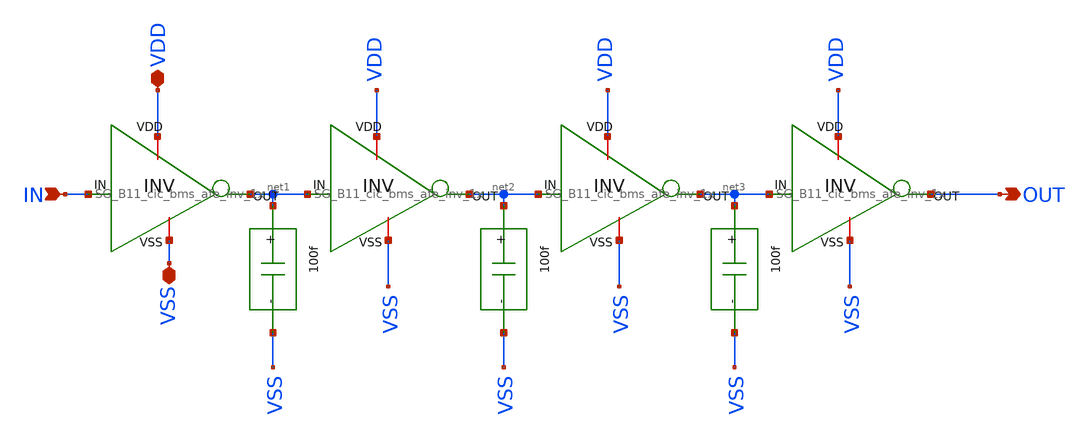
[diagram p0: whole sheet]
** sch_path: design/schematics/CCIA/Non_Overlapping_clk_gen/SG_B11_cic_bms_afe_delay_block_3n.sch
**.subckt SG_B11_cic_bms_afe_delay_block_3n IN OUT VDD VSS
*.ipin IN
*.opin OUT
*.iopin VDD
*.iopin VSS
x1 VDD net1 IN VSS SG_B11_cic_bms_afe_inv_1x
x2 VDD net2 net1 VSS SG_B11_cic_bms_afe_inv_1x
x3 VDD net3 net2 VSS SG_B11_cic_bms_afe_inv_1x
x4 VDD OUT net3 VSS SG_B11_cic_bms_afe_inv_1x
x5 net1 VSS SG_B11_cic_bms_afe_delay_3n_cap
x6 net2 VSS SG_B11_cic_bms_afe_delay_3n_cap
x7 net3 VSS SG_B11_cic_bms_afe_delay_3n_cap
**.ends
.end
